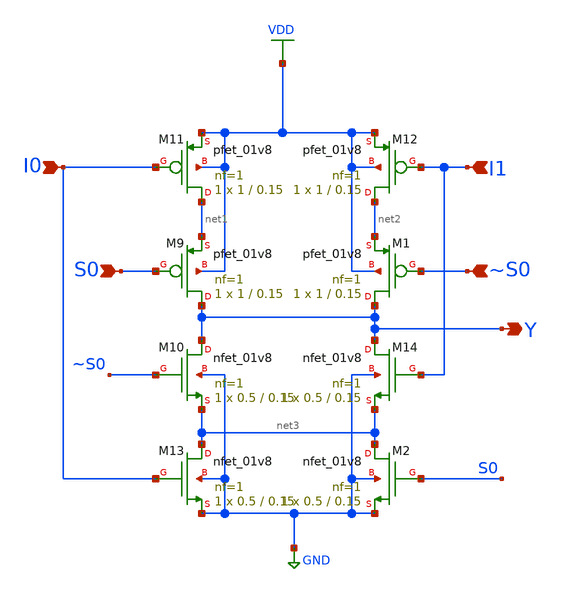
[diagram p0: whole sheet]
** sch_path: xschem/mux2.sch
**.subckt mux2 I1 I0 S0 Y ~S0
*.ipin I1
*.ipin I0
*.ipin S0
*.opin Y
*.ipin ~S0
XM9 Y S0 net1 VDD sky130_fd_pr__pfet_01v8 L=0.15 W=1 nf=1 ad='int((nf+1)/2) * W/nf * 0.29' as='int((nf+2)/2) * W/nf * 0.29'
+ pd='2*int((nf+1)/2) * (W/nf + 0.29)' ps='2*int((nf+2)/2) * (W/nf + 0.29)' nrd='0.29 / W' nrs='0.29 / W'
+ sa=0 sb=0 sd=0 mult=1 m=1
XM10 Y ~S0 net3 GND sky130_fd_pr__nfet_01v8 L=0.15 W=0.5 nf=1 ad='int((nf+1)/2) * W/nf * 0.29' as='int((nf+2)/2) * W/nf * 0.29'
+ pd='2*int((nf+1)/2) * (W/nf + 0.29)' ps='2*int((nf+2)/2) * (W/nf + 0.29)' nrd='0.29 / W' nrs='0.29 / W'
+ sa=0 sb=0 sd=0 mult=1 m=1
XM11 net1 I0 VDD VDD sky130_fd_pr__pfet_01v8 L=0.15 W=1 nf=1 ad='int((nf+1)/2) * W/nf * 0.29' as='int((nf+2)/2) * W/nf * 0.29'
+ pd='2*int((nf+1)/2) * (W/nf + 0.29)' ps='2*int((nf+2)/2) * (W/nf + 0.29)' nrd='0.29 / W' nrs='0.29 / W'
+ sa=0 sb=0 sd=0 mult=1 m=1
XM12 net2 I1 VDD VDD sky130_fd_pr__pfet_01v8 L=0.15 W=1 nf=1 ad='int((nf+1)/2) * W/nf * 0.29' as='int((nf+2)/2) * W/nf * 0.29'
+ pd='2*int((nf+1)/2) * (W/nf + 0.29)' ps='2*int((nf+2)/2) * (W/nf + 0.29)' nrd='0.29 / W' nrs='0.29 / W'
+ sa=0 sb=0 sd=0 mult=1 m=1
XM13 net3 I0 GND GND sky130_fd_pr__nfet_01v8 L=0.15 W=0.5 nf=1 ad='int((nf+1)/2) * W/nf * 0.29' as='int((nf+2)/2) * W/nf * 0.29'
+ pd='2*int((nf+1)/2) * (W/nf + 0.29)' ps='2*int((nf+2)/2) * (W/nf + 0.29)' nrd='0.29 / W' nrs='0.29 / W'
+ sa=0 sb=0 sd=0 mult=1 m=1
XM14 Y I1 net3 GND sky130_fd_pr__nfet_01v8 L=0.15 W=0.5 nf=1 ad='int((nf+1)/2) * W/nf * 0.29' as='int((nf+2)/2) * W/nf * 0.29'
+ pd='2*int((nf+1)/2) * (W/nf + 0.29)' ps='2*int((nf+2)/2) * (W/nf + 0.29)' nrd='0.29 / W' nrs='0.29 / W'
+ sa=0 sb=0 sd=0 mult=1 m=1
XM1 Y ~S0 net2 VDD sky130_fd_pr__pfet_01v8 L=0.15 W=1 nf=1 ad='int((nf+1)/2) * W/nf * 0.29' as='int((nf+2)/2) * W/nf * 0.29'
+ pd='2*int((nf+1)/2) * (W/nf + 0.29)' ps='2*int((nf+2)/2) * (W/nf + 0.29)' nrd='0.29 / W' nrs='0.29 / W'
+ sa=0 sb=0 sd=0 mult=1 m=1
XM2 net3 S0 GND GND sky130_fd_pr__nfet_01v8 L=0.15 W=0.5 nf=1 ad='int((nf+1)/2) * W/nf * 0.29' as='int((nf+2)/2) * W/nf * 0.29'
+ pd='2*int((nf+1)/2) * (W/nf + 0.29)' ps='2*int((nf+2)/2) * (W/nf + 0.29)' nrd='0.29 / W' nrs='0.29 / W'
+ sa=0 sb=0 sd=0 mult=1 m=1
**.ends
.GLOBAL VDD
.GLOBAL GND
.end
